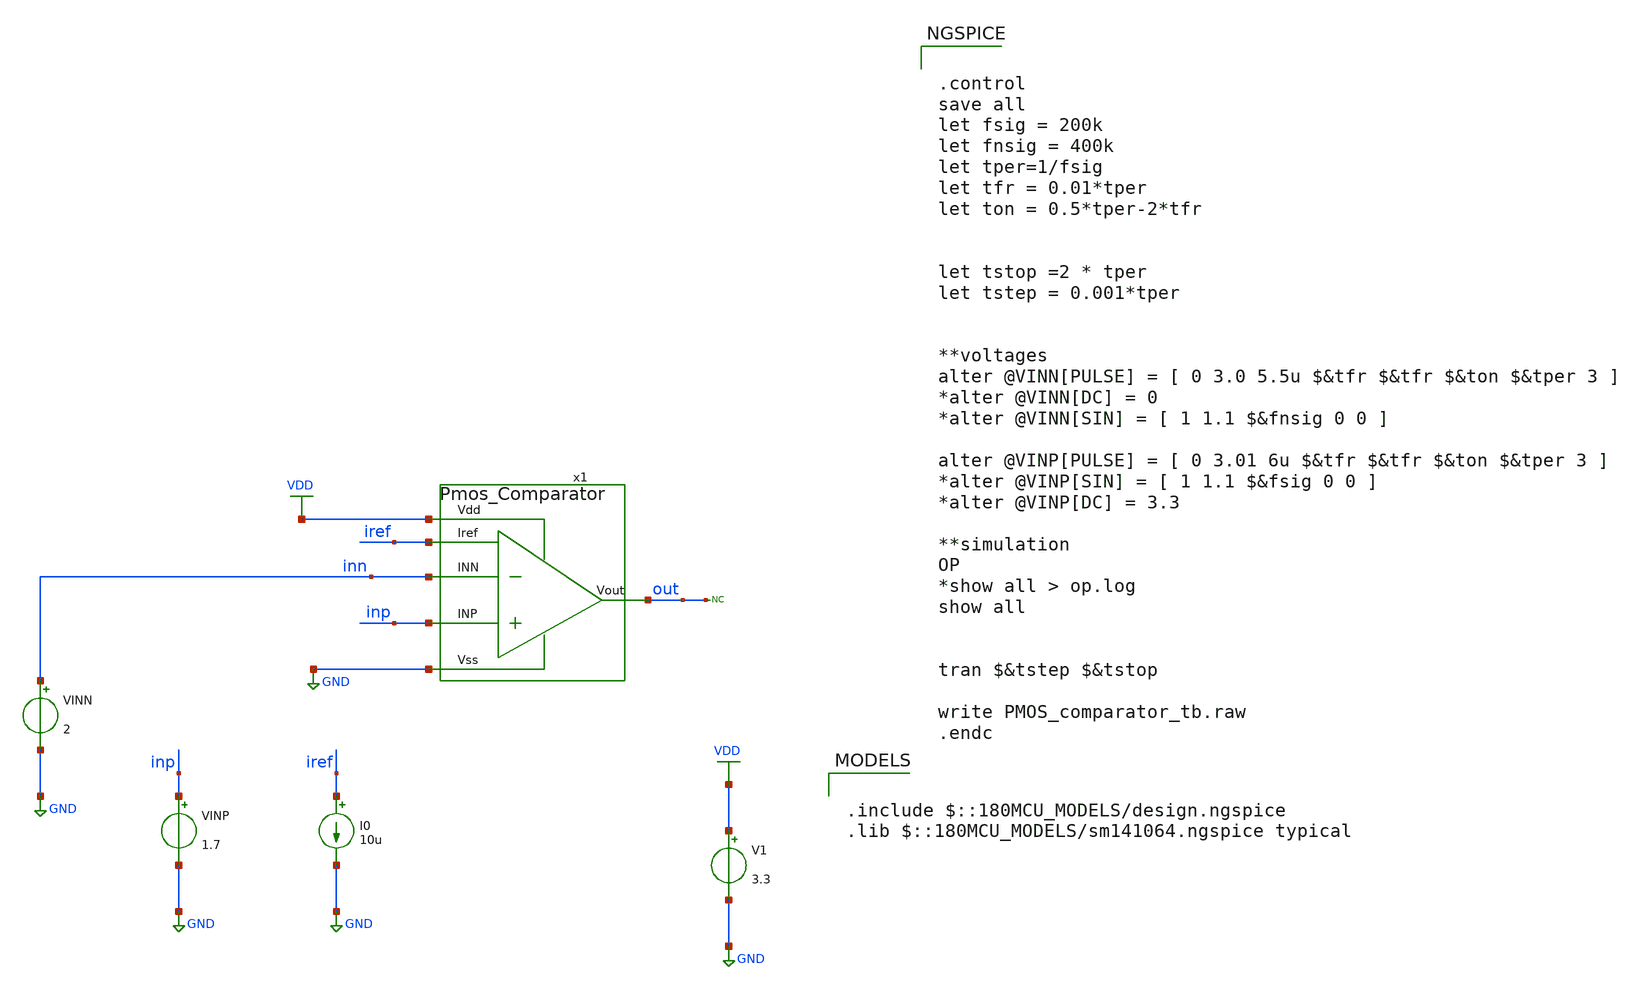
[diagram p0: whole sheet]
** sch_path: designs/libs/tb_analog/Comparator/PMOS_comparator_tb.sch
**.subckt PMOS_comparator_tb
I0 iref GND 10u
V1 VDD GND 3.3
VINP inp GND 1.7
* noconn out
VINN inn GND 2
x1 VDD iref inp out inn GND Pmos_Comparator
**** begin user architecture code


.control
save all
let fsig = 200k
let fnsig = 400k
let tper=1/fsig
let tfr = 0.01*tper
let ton = 0.5*tper-2*tfr


let tstop =2 * tper
let tstep = 0.001*tper


**voltages
alter @VINN[PULSE] = [ 0 3.0 5.5u $&tfr $&tfr $&ton $&tper 3 ]
*alter @VINN[DC] = 0
*alter @VINN[SIN] = [ 1 1.1 $&fnsig 0 0 ]

alter @VINP[PULSE] = [ 0 3.01 6u $&tfr $&tfr $&ton $&tper 3 ]
*alter @VINP[SIN] = [ 1 1.1 $&fsig 0 0 ]
*alter @VINP[DC] = 3.3

**simulation
OP
*show all > op.log
show all


tran $&tstep $&tstop

write PMOS_comparator_tb.raw
.endc



.include $::180MCU_MODELS/design.ngspice
.lib $::180MCU_MODELS/sm141064.ngspice typical

**** end user architecture code
**.ends

* expanding   symbol:  libs/core_analog/Comparator/Pmos_Comparator.sym # of pins=6
** sym_path: designs/libs/core_analog/Comparator/Pmos_Comparator.sym
** sch_path: designs/libs/core_analog/Comparator/Pmos_Comparator.sch
.subckt Pmos_Comparator Vdd Iref INP Vout INN Vss
*.ipin Vdd
*.ipin Vss
*.ipin Iref
*.ipin INN
*.ipin INP
*.opin Vout
XM3 net1 net1 Vdd Vdd pfet_03v3 L=0.6u W=5.24u nf=5 ad='int((nf+1)/2) * W/nf * 0.18u' as='int((nf+2)/2) * W/nf * 0.18u'
+ pd='2*int((nf+1)/2) * (W/nf + 0.18u)' ps='2*int((nf+2)/2) * (W/nf + 0.18u)' nrd='0.18u / W' nrs='0.18u / W'
+ sa=0 sb=0 sd=0 m=5
XM4 Vout net1 Vdd Vdd pfet_03v3 L=0.5u W=5.24u nf=5 ad='int((nf+1)/2) * W/nf * 0.18u' as='int((nf+2)/2) * W/nf * 0.18u'
+ pd='2*int((nf+1)/2) * (W/nf + 0.18u)' ps='2*int((nf+2)/2) * (W/nf + 0.18u)' nrd='0.18u / W' nrs='0.18u / W'
+ sa=0 sb=0 sd=0 m=5
XM5 net2 INN net3 Vdd pfet_03v3 L=1u W=3.24u nf=4 ad='int((nf+1)/2) * W/nf * 0.18u' as='int((nf+2)/2) * W/nf * 0.18u'
+ pd='2*int((nf+1)/2) * (W/nf + 0.18u)' ps='2*int((nf+2)/2) * (W/nf + 0.18u)' nrd='0.18u / W' nrs='0.18u / W'
+ sa=0 sb=0 sd=0 m=4
XM6 net4 INP net3 Vdd pfet_03v3 L=1u W=3.24u nf=4 ad='int((nf+1)/2) * W/nf * 0.18u' as='int((nf+2)/2) * W/nf * 0.18u'
+ pd='2*int((nf+1)/2) * (W/nf + 0.18u)' ps='2*int((nf+2)/2) * (W/nf + 0.18u)' nrd='0.18u / W' nrs='0.18u / W'
+ sa=0 sb=0 sd=0 m=4
XM7 net1 net2 Vss Vss nfet_03v3 L=1u W=5.46u nf=1 ad='int((nf+1)/2) * W/nf * 0.18u' as='int((nf+2)/2) * W/nf * 0.18u'
+ pd='2*int((nf+1)/2) * (W/nf + 0.18u)' ps='2*int((nf+2)/2) * (W/nf + 0.18u)' nrd='0.18u / W' nrs='0.18u / W'
+ sa=0 sb=0 sd=0 m=1
XM8 net2 net4 Vss Vss nfet_03v3 L=1u W=5.46u nf=4 ad='int((nf+1)/2) * W/nf * 0.18u' as='int((nf+2)/2) * W/nf * 0.18u'
+ pd='2*int((nf+1)/2) * (W/nf + 0.18u)' ps='2*int((nf+2)/2) * (W/nf + 0.18u)' nrd='0.18u / W' nrs='0.18u / W'
+ sa=0 sb=0 sd=0 m=4
XM9 net4 net4 Vss Vss nfet_03v3 L=1u W=5.46u nf=1 ad='int((nf+1)/2) * W/nf * 0.18u' as='int((nf+2)/2) * W/nf * 0.18u'
+ pd='2*int((nf+1)/2) * (W/nf + 0.18u)' ps='2*int((nf+2)/2) * (W/nf + 0.18u)' nrd='0.18u / W' nrs='0.18u / W'
+ sa=0 sb=0 sd=0 m=1
XM10 net4 net2 Vss Vss nfet_03v3 L=1u W=5.46u nf=4 ad='int((nf+1)/2) * W/nf * 0.18u' as='int((nf+2)/2) * W/nf * 0.18u'
+ pd='2*int((nf+1)/2) * (W/nf + 0.18u)' ps='2*int((nf+2)/2) * (W/nf + 0.18u)' nrd='0.18u / W' nrs='0.18u / W'
+ sa=0 sb=0 sd=0 m=4
XM11 net2 net2 Vss Vss nfet_03v3 L=1u W=5.46u nf=1 ad='int((nf+1)/2) * W/nf * 0.18u' as='int((nf+2)/2) * W/nf * 0.18u'
+ pd='2*int((nf+1)/2) * (W/nf + 0.18u)' ps='2*int((nf+2)/2) * (W/nf + 0.18u)' nrd='0.18u / W' nrs='0.18u / W'
+ sa=0 sb=0 sd=0 m=1
XM12 Vout net4 Vss Vss nfet_03v3 L=1u W=5.46u nf=1 ad='int((nf+1)/2) * W/nf * 0.18u' as='int((nf+2)/2) * W/nf * 0.18u'
+ pd='2*int((nf+1)/2) * (W/nf + 0.18u)' ps='2*int((nf+2)/2) * (W/nf + 0.18u)' nrd='0.18u / W' nrs='0.18u / W'
+ sa=0 sb=0 sd=0 m=1
x1 Vdd Vdd Iref Iref unit_pmos M=2
x2 Vdd Vdd Iref net3 unit_pmos M=4
.ends


* expanding   symbol:  libs/core_analog/unit_pmos/unit_pmos.sym # of pins=4
** sym_path: libs/core_analog/unit_pmos/unit_pmos.sym
** sch_path: libs/core_analog/unit_pmos/unit_pmos.sch
.subckt unit_pmos drain sub gate source
*.iopin drain
*.iopin source
*.iopin sub
*.iopin gate
**** begin user architecture code

.param M=1

**** end user architecture code
XM3 drain gate source sub pfet_03v3 L=1u W=3.5u nf=1 ad='int((nf+1)/2) * W/nf * 0.18u' as='int((nf+2)/2) * W/nf * 0.18u'
+ pd='2*int((nf+1)/2) * (W/nf + 0.18u)' ps='2*int((nf+2)/2) * (W/nf + 0.18u)' nrd='0.18u / W' nrs='0.18u / W'
+ sa=0 sb=0 sd=0 m={M}
.ends

.GLOBAL GND
.GLOBAL VDD
.end
